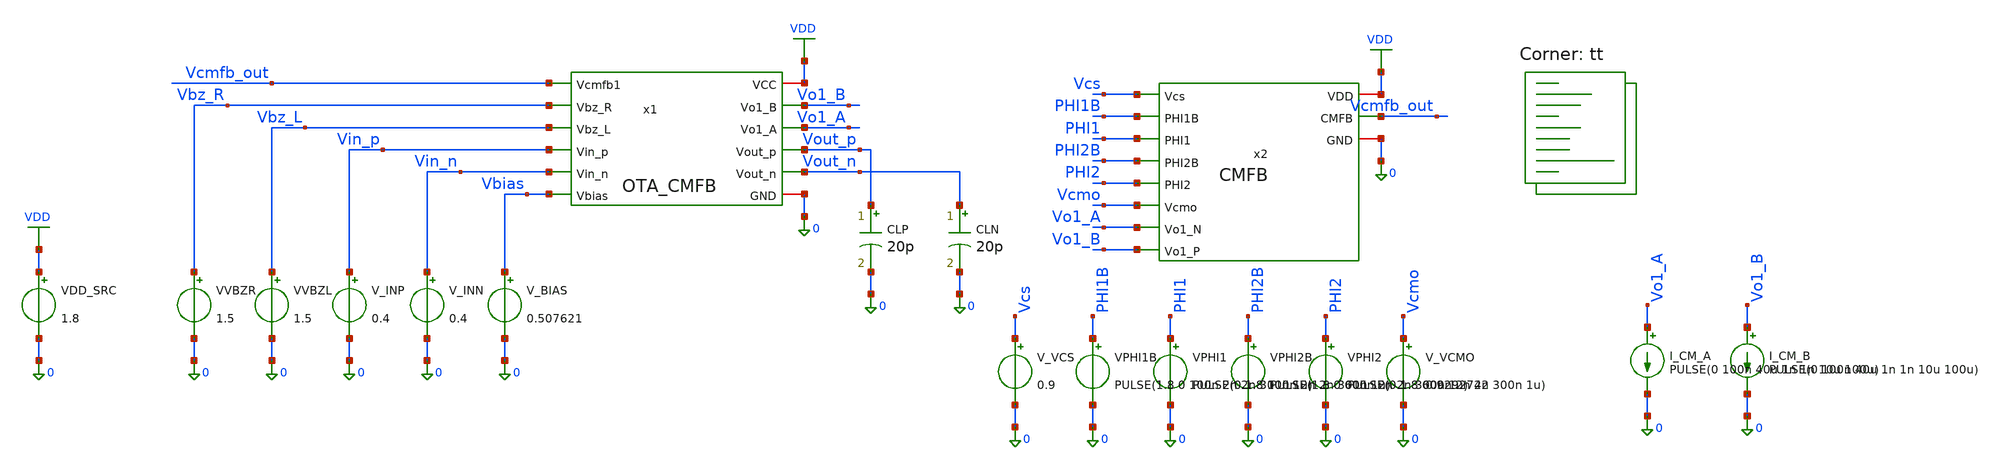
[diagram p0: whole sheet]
** sch_path: blocks/02_CMFB/sim/tb_CMFB_STABILITY_100nA_CMstep_TT.sch
**.subckt tb_CMFB_STABILITY_100nA_CMstep_TT
x1 VDD Vcmfb_out Vbz_R Vbz_L Vin_p Vin_n Vo1_B Vo1_A Vout_p Vout_n Vbias 0 OTA_CMFB
x2 Vcmfb_out Vcs PHI1B PHI1 VDD PHI2B 0 PHI2 Vcmo Vo1_A Vo1_B CMFB
VDD_SRC VDD 0 1.8
VVBZR Vbz_R 0 1.5
VVBZL Vbz_L 0 1.5
V_INP Vin_p 0 0.4
V_INN Vin_n 0 0.4
V_BIAS Vbias 0 0.507621
CLP Vout_p 0 20p m=1
CLN Vout_n 0 20p m=1
V_VCS Vcs 0 0.9
VPHI1B PHI1B 0 PULSE(1.8 0 100n 2n 2n 300n 1u)
VPHI1 PHI1 0 PULSE(0 1.8 100n 2n 2n 300n 1u)
VPHI2B PHI2B 0 PULSE(1.8 0 600n 2n 2n 300n 1u)
VPHI2 PHI2 0 PULSE(0 1.8 600n 2n 2n 300n 1u)
V_VCMO Vcmo 0 0.9292742
I_CM_A Vo1_A 0 PULSE(0 100n 40u 1n 1n 10u 100u)
I_CM_B Vo1_B 0 PULSE(0 100n 40u 1n 1n 10u 100u)
**** begin user architecture code
.lib $::SKYWATER_MODELS/sky130.lib.spice tt


* Common-mode current disturbance applied to both first-stage nodes.
* Simulate at TT, 27C, 1.8V with 100nA drawn from each node,
* from 40us to 50us. No direct ideal voltage forcing of first-stage outputs.
.temp 27
.options rshunt=1e12
RLEAK_CMFB Vcmfb_out 0 1e12
.control
save all
tran 1n 100u
let vo1cm = (v(vo1_a)+v(vo1_b))/2
let vocm = (v(vout_p)+v(vout_n))/2
meas tran CM_BASE AVG vo1cm FROM=30u TO=39u
meas tran CM_DURING AVG vo1cm FROM=42u TO=49u
meas tran CM_RECOVER AVG vo1cm FROM=90u TO=100u
meas tran CM_REC_MIN MIN vo1cm FROM=90u TO=100u
meas tran CM_REC_MAX MAX vo1cm FROM=90u TO=100u
meas tran CTRL_BASE AVG v(vcmfb_out) FROM=30u TO=39u
meas tran CTRL_DURING AVG v(vcmfb_out) FROM=42u TO=49u
meas tran CTRL_RECOVER AVG v(vcmfb_out) FROM=90u TO=100u
meas tran OUT_BASE AVG vocm FROM=30u TO=39u
meas tran OUT_DURING AVG vocm FROM=42u TO=49u
meas tran OUT_RECOVER AVG vocm FROM=90u TO=100u
let CM_DISTURBANCE = CM_DURING-CM_BASE
let CM_RECOVERY_ERR = CM_RECOVER-CM_BASE
let CM_REC_RIPPLE = CM_REC_MAX-CM_REC_MIN
let CTRL_RESPONSE = CTRL_DURING-CTRL_BASE
let CTRL_RECOVERY_ERR = CTRL_RECOVER-CTRL_BASE
let OUT_RESPONSE = OUT_DURING-OUT_BASE
let OUT_RECOVERY_ERR = OUT_RECOVER-OUT_BASE
echo ===== CLOSED LOOP COMMON MODE DISTURBANCE =====
print CM_BASE CM_DURING CM_RECOVER
print CM_DISTURBANCE CM_RECOVERY_ERR CM_REC_RIPPLE
print CTRL_BASE CTRL_DURING CTRL_RECOVER
print CTRL_RESPONSE CTRL_RECOVERY_ERR
print OUT_BASE OUT_DURING OUT_RECOVER
print OUT_RESPONSE OUT_RECOVERY_ERR
plot vo1cm
plot v(vcmfb_out)
plot vocm
.endc


**** end user architecture code
**.ends
.GLOBAL VDD
.end
